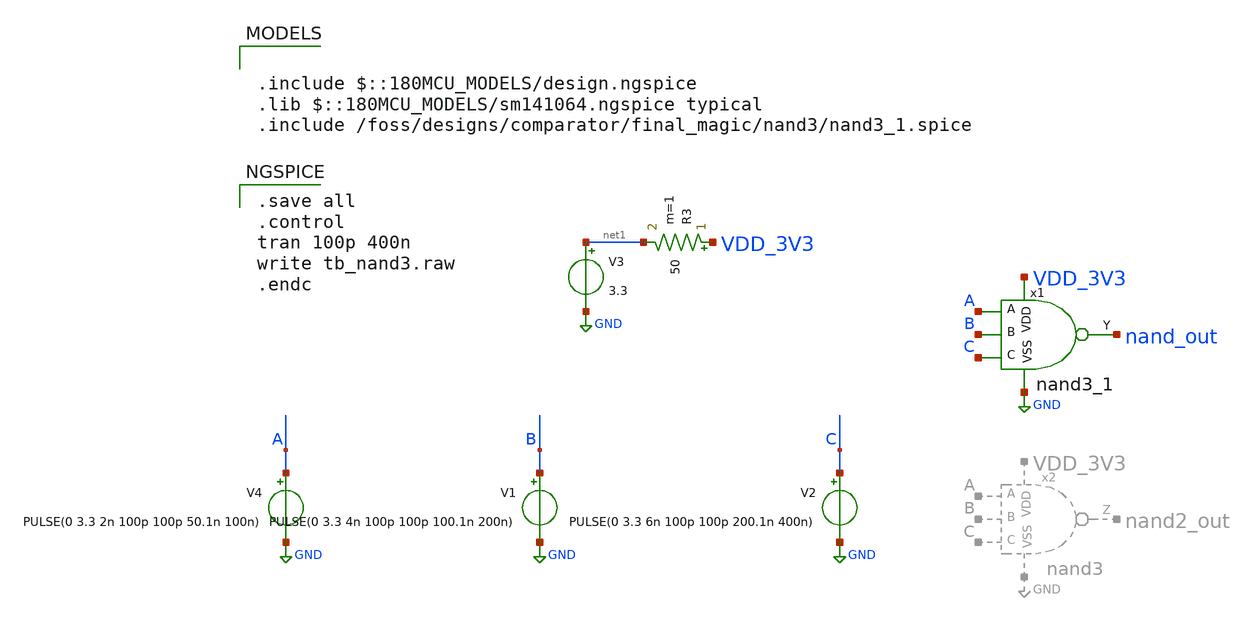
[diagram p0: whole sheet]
** sch_path: designs/comparator/final_magic/osu_sc/nand3/tb_nand3.sch
**.subckt tb_nand3
V4 A GND PULSE(0 3.3 2n 100p 100p 50.1n 100n)
V1 B GND PULSE(0 3.3 4n 100p 100p 100.1n 200n)
V2 C GND PULSE(0 3.3 6n 100p 100p 200.1n 400n)
x1 C A B nand_out VDD_3V3 GND nand3_1
V3 net1 GND 3.3
R3 VDD_3V3 net1 50 m=1
**** begin user architecture code

.include $::180MCU_MODELS/design.ngspice
.lib $::180MCU_MODELS/sm141064.ngspice typical
.include /foss/designs/comparator/final_magic/nand3/nand3_1.spice


.save all
.control
tran 100p 400n
write tb_nand3.raw
.endc

**** end user architecture code
**.ends
.GLOBAL GND
.end
